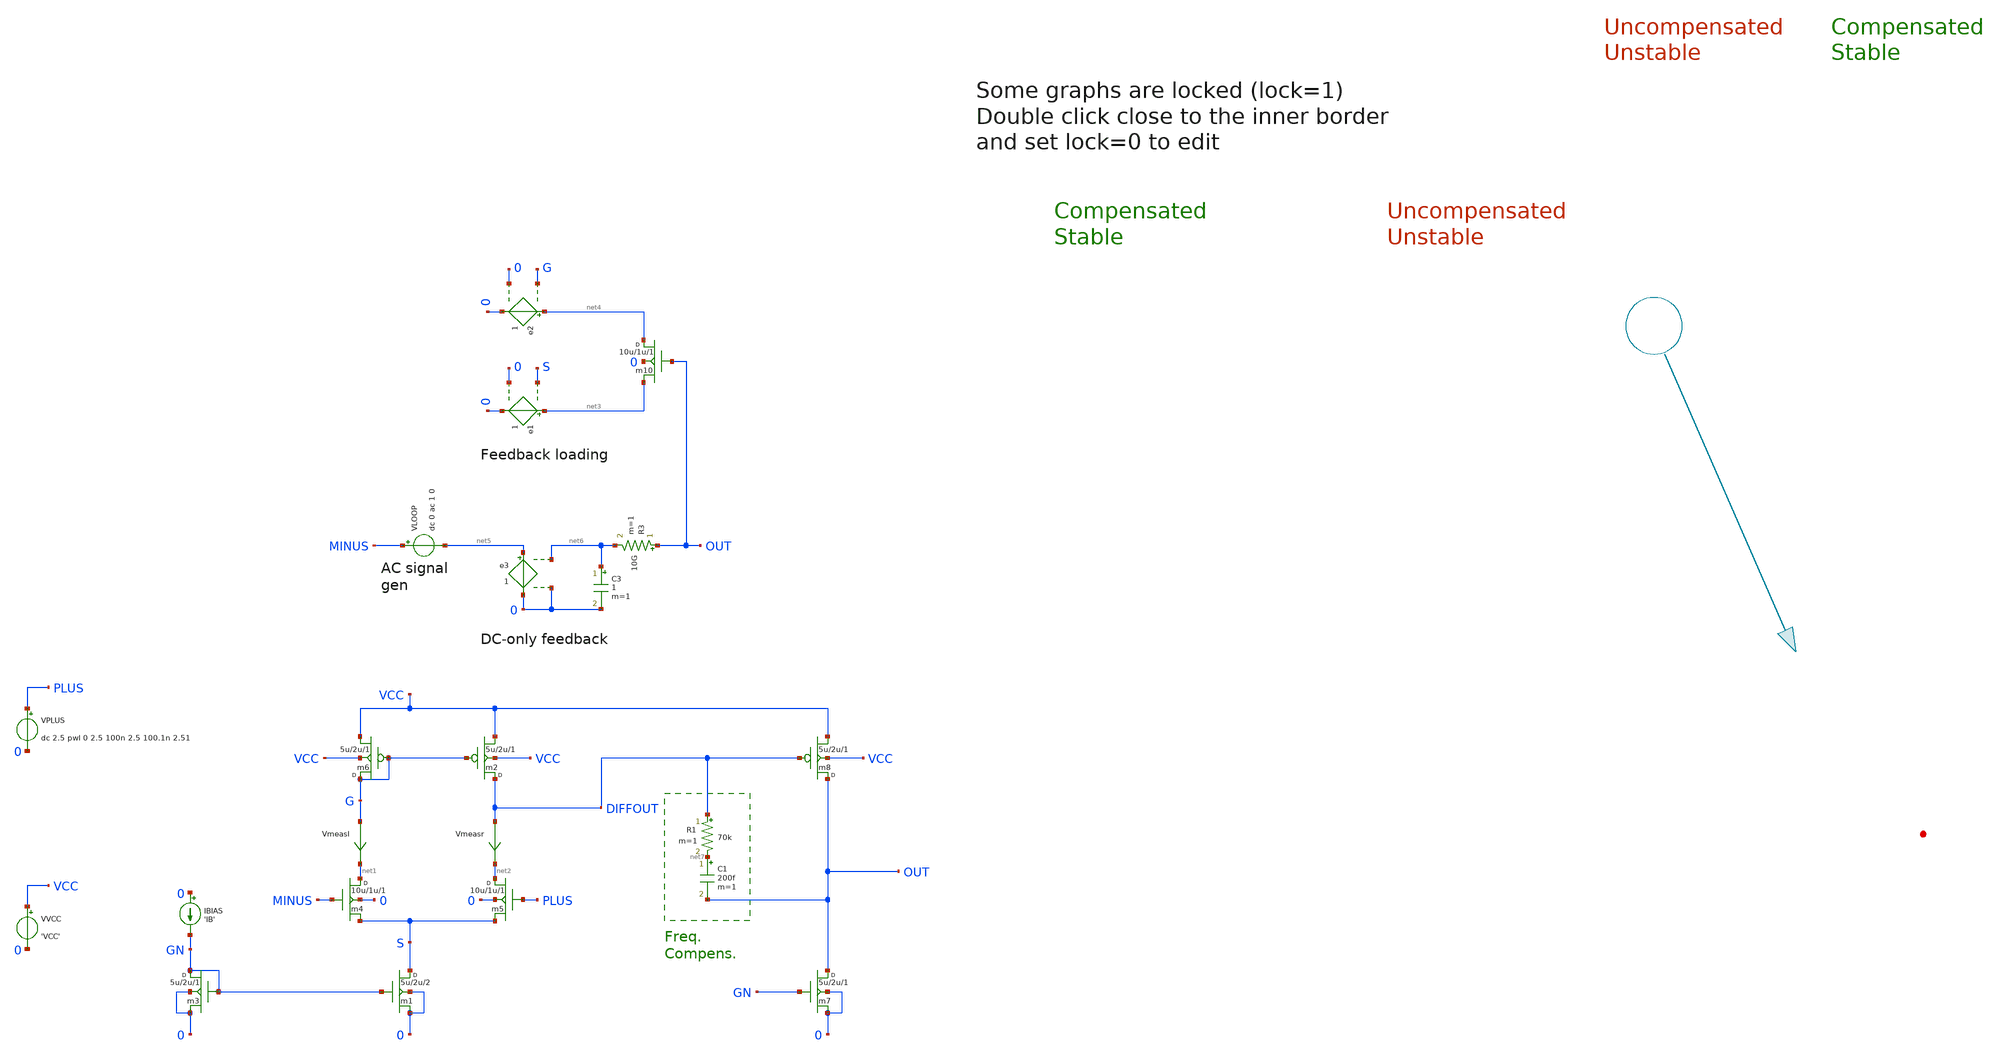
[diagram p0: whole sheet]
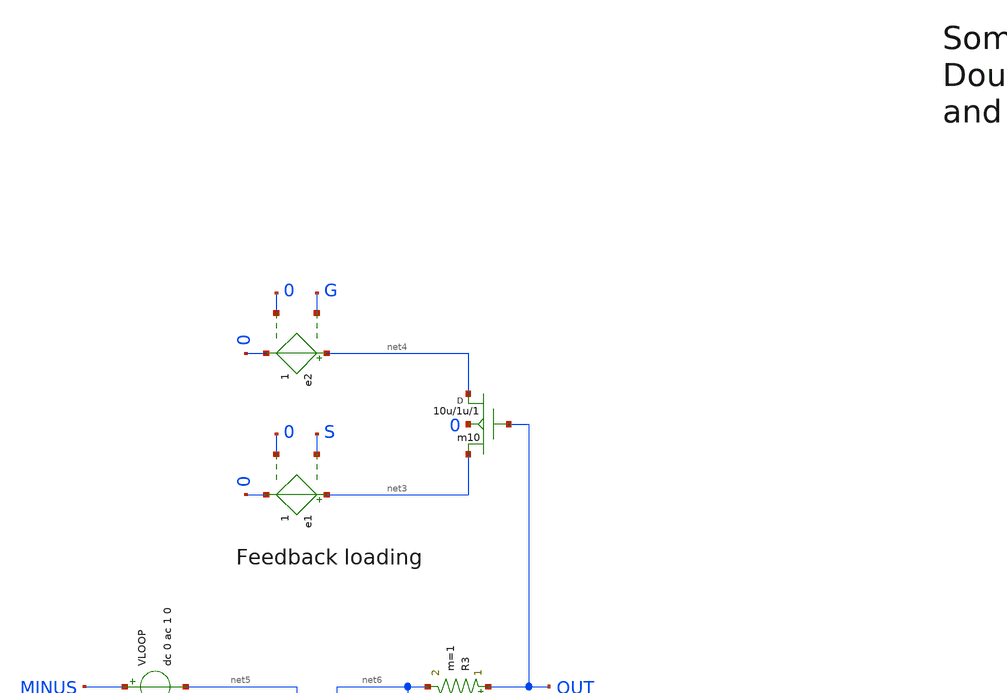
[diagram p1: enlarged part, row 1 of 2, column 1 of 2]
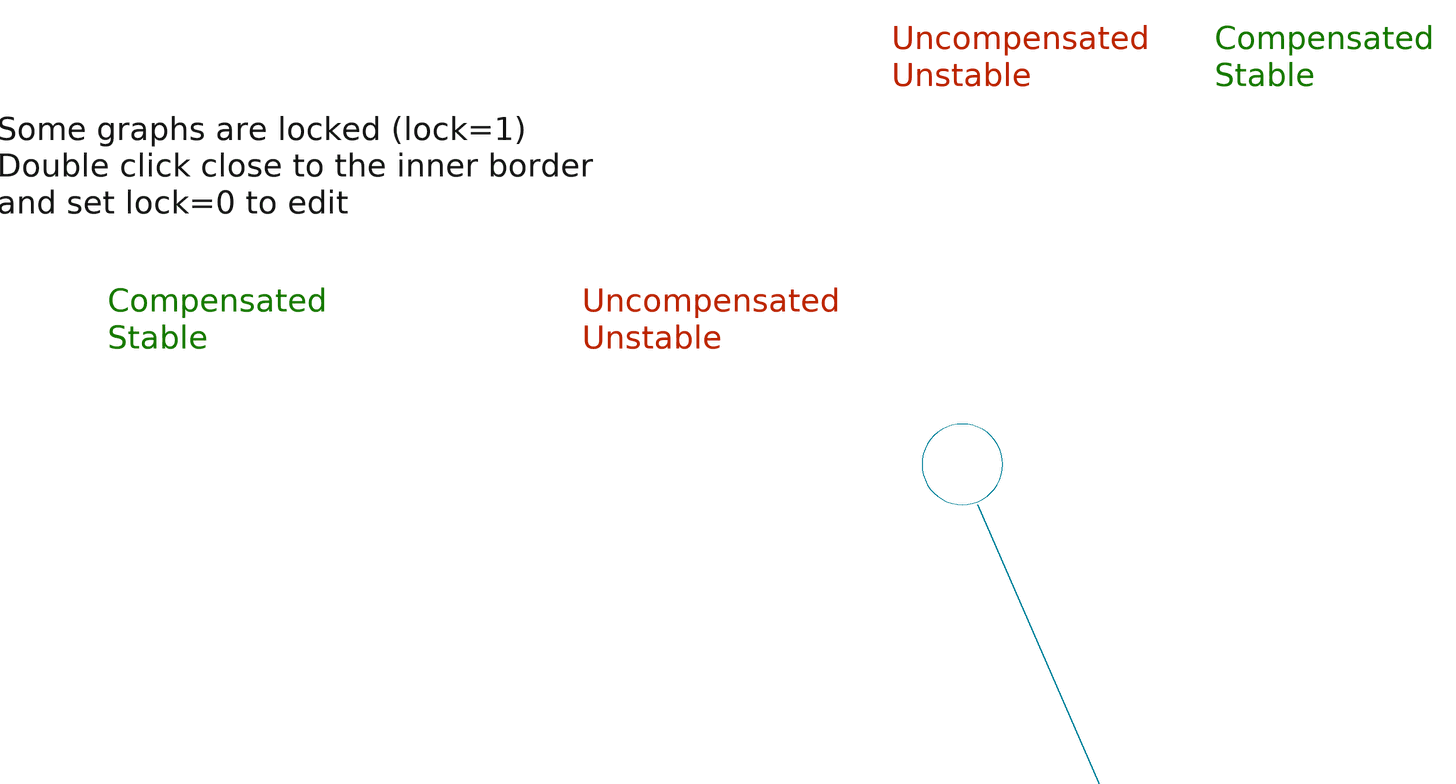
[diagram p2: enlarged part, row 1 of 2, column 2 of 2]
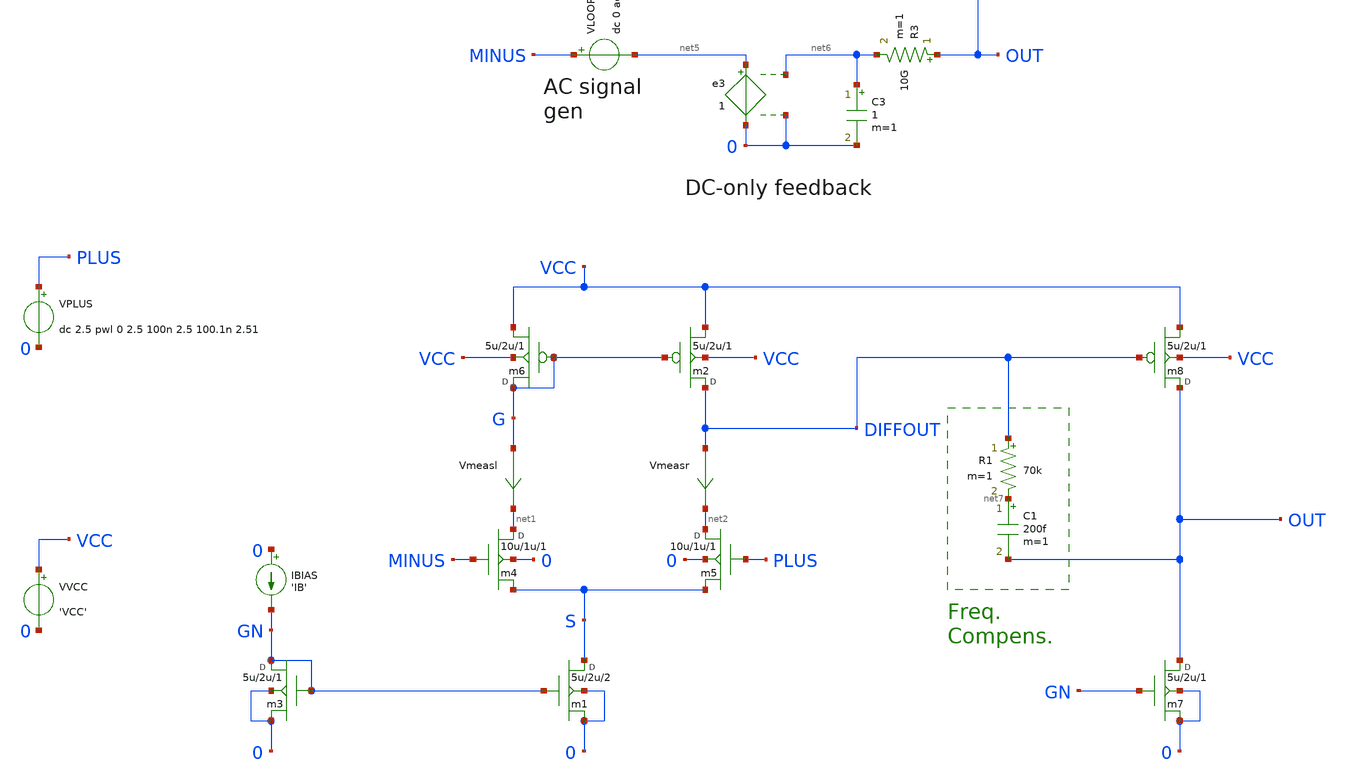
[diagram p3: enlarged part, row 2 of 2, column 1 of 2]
** sch_path: tests/test_sweep_diff/examples/test_nyquist/schematic/test_nyquist.sch
* Copyright (C) 1998-2024 Stefan Frederik Schippers
* This program is free software; you can redistribute it and/or modify
* it under the terms of the GNU General Public License as published by
* the Free Software Foundation; either version 2 of the License, or
* (at your option) any later version.
* This program is distributed in the hope that it will be useful,
* but WITHOUT ANY WARRANTY; without even the implied warranty of
* MERCHANTABILITY or FITNESS FOR A PARTICULAR PURPOSE.  See the
* GNU General Public License for more details.
* You should have received a copy of the GNU General Public License
* along with this program; if not, write to the Free Software
**.subckt test_nyquist
m1 S GN 0 0 cmosn w=5u l=2u m=2
m2 DIFFOUT G VCC VCC cmosp w=5u l=2u m=1
VVCC VCC 0 'VCC'
m3 GN GN 0 0 cmosn w=5u l=2u m=1
IBIAS 0 GN 'IB'
m4 net1 MINUS S 0 cmosn w=10u l=1u m=1
m5 net2 PLUS S 0 cmosn w=10u l=1u m=1
m6 G G VCC VCC cmosp w=5u l=2u m=1
VPLUS PLUS 0 dc 2.5 pwl 0 2.5 100n 2.5 100.1n 2.51
Vmeasr DIFFOUT net2 0
.save i(vmeasr)
Vmeasl G net1 0
.save i(vmeasl)
m7 OUT GN 0 0 cmosn w=5u l=2u m=1
m8 OUT DIFFOUT VCC VCC cmosp w=5u l=2u m=1
R1 DIFFOUT net7 70k m=1
C1 net7 OUT 200f m=1
e1 net3 0 S 0 1
e2 net4 0 G 0 1
m10 net4 OUT net3 0 cmosn w=10u l=1u m=1
R3 OUT net6 10G m=1
C3 net6 0 1 m=1
e3 net5 0 net6 0 1
VLOOP MINUS net5 dc 0 ac 1 0
**** begin user architecture code


.temp 30
.param IB=2u GMIN=1e-16
.param VCC = 5
.option savecurrents
.control
   save all
   op
   remzerovec
   write test_nyquist.raw
   set appendwrite
   ac dec 100 1 10G
   * tran 0.1n 1u
   remzerovec
   write test_nyquist.raw

   alter R1=5000G
   alter C1=1a

   ac dec 100 1 10G
   * tran 0.1n 1u
   remzerovec
   write test_nyquist.raw



   quit 0
.endc




**** end user architecture code
**.ends
**** begin user architecture code

*p-ch model
.MODEL CMOSP PMOS ( LEVEL   = 49             acm     = 3 VERSION = 3.1            TNOM    = 27
+             TOX     = 7.7E-9 XJ      = 1E-7           NCH     = 8.52E16        VTH0    = -0.6897992 K1      =
+ 0.4134289      K2      = -5.342989E-3   K3      = 24.8361788 K3B     = -1.4390847     W0      = 2.467689E-6
+    NLX     = 3.096223E-7 DVT0W   = 0              DVT1W   = 0              DVT2W   = 0 DVT0    = 1.3209807
+      DVT1    = 0.4695965      DVT2    = -8.790762E-4 U0      = 150.6275733    UA      = 2.016943E-10   UB
+      = 1.714919E-18 UC      = -1.36948E-11   VSAT    = 9.559222E4     A0      = 0.9871247 AGS     =
+ 0.3541967      B0      = 3.188091E-6    B1      = 5E-6 KETA    = -0.0169877     A1      = 0              A2
+      = 1 RDSW    = 2.443009E3     PRWG    = 0.0260616      PRWB    = 0.141561 WR      = 1
+              WINT    = 5.038936E-8    LINT    = 1.650588E-9 XL      = -2E-8          XW      = 0              DWG
+     = -1.535456E-8 DWB     = 1.256904E-8    VOFF    = -0.15          NFACTOR = 1.5460516 CIT     = 0
+              CDSC    = 1.413317E-4    CDSCD   = 0 CDSCB   = 0              ETA0    = 0.3751392      ETAB    =
+ 2.343374E-3 DSUB    = 0.8877574      PCLM    = 5.8638076      PDIBLC1 = 1.05224E-3 PDIBLC2 = 3.481753E-5
+    PDIBLCB = 2.37525E-3     DROUT   = 0.0277454 PSCBE1  = 3.013379E10    PSCBE2  = 3.608179E-8    PVAG    =
+ 3.9564294 DELTA   = 0.01           MOBMOD  = 1              PRT     = 0 UTE     = -1.5           KT1     =
+ -0.11          KT1L    = 0 KT2     = 0.022          UA1     = 4.31E-9        UB1     = -7.61E-18 UC1
+     = -5.6E-11       AT      = 3.3E4          WL      = 0 WLN     = 1              WW      = -5.22182E-16
+   WWN     = 1.125 WWL     = 0              LL      = 0              LLN     = 1 LW      = 0
+              LWN     = 1              LWL     = 0 CAPMOD  = 2              XPART   = 0.4            CGDO    =
+ 2.307E-10 CGSO    = 2.307E-10      CGBO    = 0              CJ      = 1.397645E-3 PB      = 0.99           MJ
+      = 0.5574537      CJSW    = 3.665392E-10 PBSW    = 0.99           MJSW    = 0.3399328      PVTH0   =
+ 0.0114364 PRDSW   = 52.7951169     PK2     = 9.714153E-4    WKETA   = 0.0109418 LKETA   = 7.702974E-3     )


*n-ch model
.MODEL CMOSN NMOS ( LEVEL   = 49             acm     = 3 VERSION = 3.1            TNOM    = 27
+             TOX     = 7.7E-9 XJ      = 1E-7           NCH     = 2.3579E17      VTH0    = 0.5048265 K1      =
+ 0.5542796      K2      = 0.0155863      K3      = 2.3475646 K3B     = -3.3142916     W0      = 4.145888E-5
+    NLX     = 1.430868E-7 DVT0W   = 0              DVT1W   = 0              DVT2W   = 0 DVT0    =
+ -0.0150839     DVT1    = 1.51022E-3     DVT2    = 0.170688 U0      = 415.8570638    UA      = 5.057324E-11
+   UB      = 1.496793E-18 UC      = 2.986268E-11   VSAT    = 1.237033E5     A0      = 0.9098788 AGS     =
+ 0.2120181      B0      = 1.683612E-6    B1      = 5E-6 KETA    = -4.011887E-4   A1      = 0              A2
+      = 1 RDSW    = 1.156967E3     PRWG    = -8.468558E-3   PRWB    = -7.678669E-3 WR      = 1
+              WINT    = 5.621821E-8    LINT    = 1.606205E-8 XL      = -2E-8          XW      = 0              DWG
+     = -6.450939E-9 DWB     = 6.530228E-9    VOFF    = -0.1259348     NFACTOR = 0.3344887 CIT     = 0
+              CDSC    = 1.527511E-3    CDSCD   = 0 CDSCB   = 0              ETA0    = 1.21138E-3     ETAB    =
+ -1.520242E-4 DSUB    = 0.1259886      PCLM    = 0.8254768      PDIBLC1 = 0.4211084 PDIBLC2 = 6.081164E-3
+    PDIBLCB = -5.865856E-6   DROUT   = 0.7022263 PSCBE1  = 7.238634E9     PSCBE2  = 5E-10          PVAG    =
+ 0.6261655 DELTA   = 0.01           MOBMOD  = 1              PRT     = 0 UTE     = -1.5           KT1     =
+ -0.11          KT1L    = 0 KT2     = 0.022          UA1     = 4.31E-9        UB1     = -7.61E-18 UC1
+     = -5.6E-11       AT      = 3.3E4          WL      = 0 WLN     = 1              WW      = -1.22182E-15
+   WWN     = 1.137 WWL     = 0              LL      = 0              LLN     = 1 LW      = 0
+              LWN     = 1              LWL     = 0 CAPMOD  = 2              XPART   = 0.4            CGDO    =
+ 1.96E-10 CGSO    = 1.96E-10       CGBO    = 0              CJ      = 8.829973E-4 PB      = 0.7946332      MJ
+      = 0.3539285      CJSW    = 2.992362E-10 PBSW    = 0.9890846      MJSW    = 0.1871372      PVTH0   =
+ -0.0148617 PRDSW   = -114.7860236   PK2     = -5.151187E-3   WKETA   = 5.687313E-3 LKETA   = -0.018518       )

**** end user architecture code
.end
